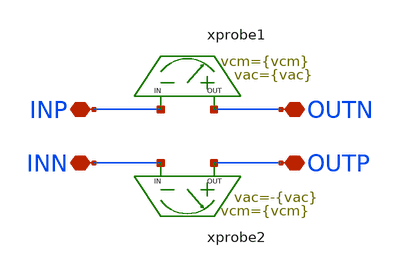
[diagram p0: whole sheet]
** sch_path: schema/ac_diff_probe/ac_diff_probe.sch
**.subckt ac_diff_probe OUTN INP OUTP INN
*.iopin OUTN
*.iopin INP
*.iopin OUTP
*.iopin INN
xprobe1 OUTN INP ac_probe vcm={vcm} vac={vac}
xprobe2 OUTP INN ac_probe vcm={vcm} vac=-{vac}
**.ends

* expanding   symbol:  ac_probe/ac_probe.sym # of pins=2
** sym_path: schema/ac_probe/ac_probe.sym
** sch_path: schema/ac_probe/ac_probe.sch
.subckt ac_probe OUT IN  vcm=0.75 vac=0.01

*.iopin IN
*.iopin OUT
C1 0 IN 1 m=1
V1 IN 0 {vcm} ac {vac}
R1 OUT IN 1G m=1
.ends

.end
